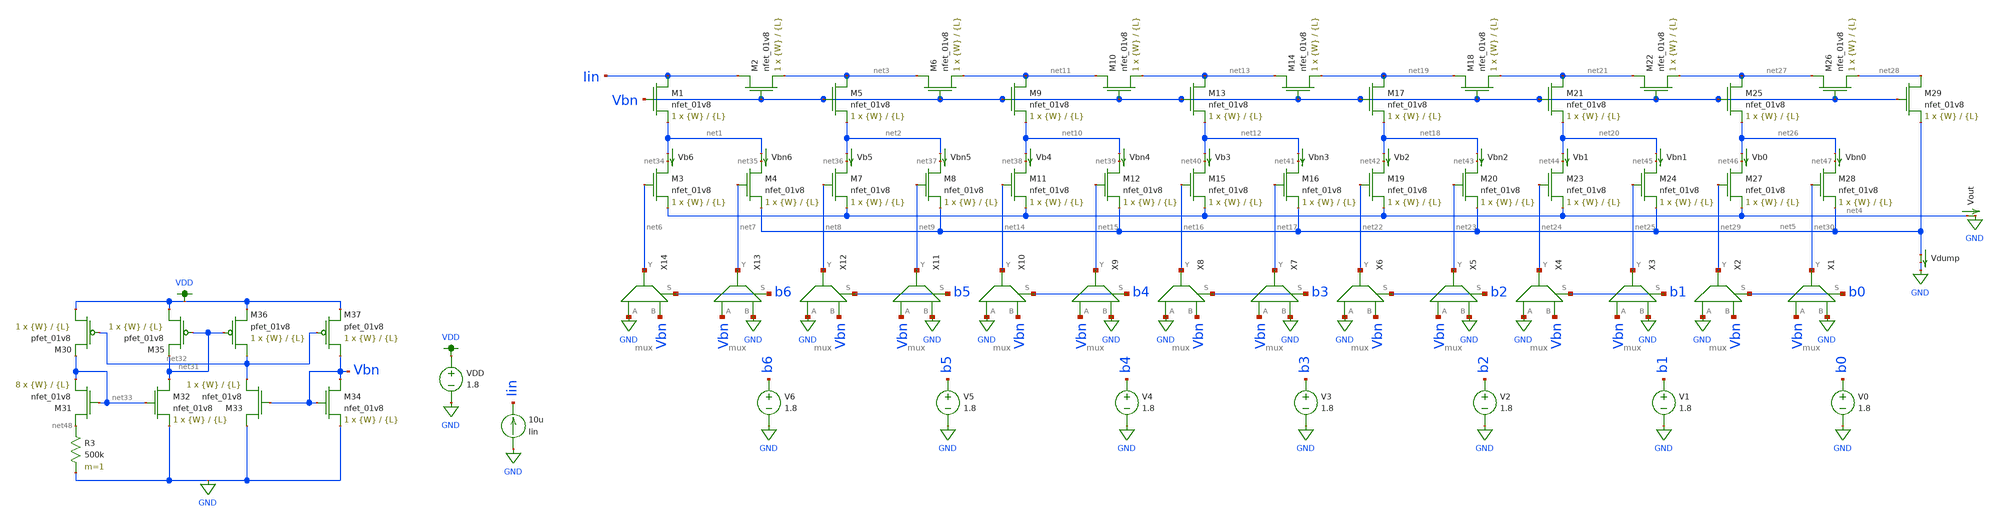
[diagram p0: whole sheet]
** sch_path: schematics/dac_from_paper.sch
**.subckt dac_from_paper
XM1 Iin Vbn net1 GND sky130_fd_pr__nfet_01v8 L={L} W={W} nf=1 ad='int((nf+1)/2) * W/nf * 0.29' as='int((nf+2)/2) * W/nf * 0.29'
+ pd='2*int((nf+1)/2) * (W/nf + 0.29)' ps='2*int((nf+2)/2) * (W/nf + 0.29)' nrd='0.29 / W' nrs='0.29 / W'
+ sa=0 sb=0 sd=0 mult=1 m=1
XM2 Iin Vbn net3 GND sky130_fd_pr__nfet_01v8 L={L} W={W} nf=1 ad='int((nf+1)/2) * W/nf * 0.29' as='int((nf+2)/2) * W/nf * 0.29'
+ pd='2*int((nf+1)/2) * (W/nf + 0.29)' ps='2*int((nf+2)/2) * (W/nf + 0.29)' nrd='0.29 / W' nrs='0.29 / W'
+ sa=0 sb=0 sd=0 mult=1 m=1
XM3 net34 net6 net4 GND sky130_fd_pr__nfet_01v8 L={L} W={W} nf=1 ad='int((nf+1)/2) * W/nf * 0.29' as='int((nf+2)/2) * W/nf * 0.29'
+ pd='2*int((nf+1)/2) * (W/nf + 0.29)' ps='2*int((nf+2)/2) * (W/nf + 0.29)' nrd='0.29 / W' nrs='0.29 / W'
+ sa=0 sb=0 sd=0 mult=1 m=1
XM4 net35 net7 net5 GND sky130_fd_pr__nfet_01v8 L={L} W={W} nf=1 ad='int((nf+1)/2) * W/nf * 0.29' as='int((nf+2)/2) * W/nf * 0.29'
+ pd='2*int((nf+1)/2) * (W/nf + 0.29)' ps='2*int((nf+2)/2) * (W/nf + 0.29)' nrd='0.29 / W' nrs='0.29 / W'
+ sa=0 sb=0 sd=0 mult=1 m=1
XM5 net3 Vbn net2 GND sky130_fd_pr__nfet_01v8 L={L} W={W} nf=1 ad='int((nf+1)/2) * W/nf * 0.29' as='int((nf+2)/2) * W/nf * 0.29'
+ pd='2*int((nf+1)/2) * (W/nf + 0.29)' ps='2*int((nf+2)/2) * (W/nf + 0.29)' nrd='0.29 / W' nrs='0.29 / W'
+ sa=0 sb=0 sd=0 mult=1 m=1
XM6 net3 Vbn net11 GND sky130_fd_pr__nfet_01v8 L={L} W={W} nf=1 ad='int((nf+1)/2) * W/nf * 0.29' as='int((nf+2)/2) * W/nf * 0.29'
+ pd='2*int((nf+1)/2) * (W/nf + 0.29)' ps='2*int((nf+2)/2) * (W/nf + 0.29)' nrd='0.29 / W' nrs='0.29 / W'
+ sa=0 sb=0 sd=0 mult=1 m=1
XM7 net36 net8 net4 GND sky130_fd_pr__nfet_01v8 L={L} W={W} nf=1 ad='int((nf+1)/2) * W/nf * 0.29' as='int((nf+2)/2) * W/nf * 0.29'
+ pd='2*int((nf+1)/2) * (W/nf + 0.29)' ps='2*int((nf+2)/2) * (W/nf + 0.29)' nrd='0.29 / W' nrs='0.29 / W'
+ sa=0 sb=0 sd=0 mult=1 m=1
XM8 net37 net9 net5 GND sky130_fd_pr__nfet_01v8 L={L} W={W} nf=1 ad='int((nf+1)/2) * W/nf * 0.29' as='int((nf+2)/2) * W/nf * 0.29'
+ pd='2*int((nf+1)/2) * (W/nf + 0.29)' ps='2*int((nf+2)/2) * (W/nf + 0.29)' nrd='0.29 / W' nrs='0.29 / W'
+ sa=0 sb=0 sd=0 mult=1 m=1
XM9 net11 Vbn net10 GND sky130_fd_pr__nfet_01v8 L={L} W={W} nf=1 ad='int((nf+1)/2) * W/nf * 0.29' as='int((nf+2)/2) * W/nf * 0.29'
+ pd='2*int((nf+1)/2) * (W/nf + 0.29)' ps='2*int((nf+2)/2) * (W/nf + 0.29)' nrd='0.29 / W' nrs='0.29 / W'
+ sa=0 sb=0 sd=0 mult=1 m=1
XM10 net11 Vbn net13 GND sky130_fd_pr__nfet_01v8 L={L} W={W} nf=1 ad='int((nf+1)/2) * W/nf * 0.29' as='int((nf+2)/2) * W/nf * 0.29'
+ pd='2*int((nf+1)/2) * (W/nf + 0.29)' ps='2*int((nf+2)/2) * (W/nf + 0.29)' nrd='0.29 / W' nrs='0.29 / W'
+ sa=0 sb=0 sd=0 mult=1 m=1
XM11 net38 net14 net4 GND sky130_fd_pr__nfet_01v8 L={L} W={W} nf=1 ad='int((nf+1)/2) * W/nf * 0.29' as='int((nf+2)/2) * W/nf * 0.29'
+ pd='2*int((nf+1)/2) * (W/nf + 0.29)' ps='2*int((nf+2)/2) * (W/nf + 0.29)' nrd='0.29 / W' nrs='0.29 / W'
+ sa=0 sb=0 sd=0 mult=1 m=1
XM12 net39 net15 net5 GND sky130_fd_pr__nfet_01v8 L={L} W={W} nf=1 ad='int((nf+1)/2) * W/nf * 0.29' as='int((nf+2)/2) * W/nf * 0.29'
+ pd='2*int((nf+1)/2) * (W/nf + 0.29)' ps='2*int((nf+2)/2) * (W/nf + 0.29)' nrd='0.29 / W' nrs='0.29 / W'
+ sa=0 sb=0 sd=0 mult=1 m=1
XM13 net13 Vbn net12 GND sky130_fd_pr__nfet_01v8 L={L} W={W} nf=1 ad='int((nf+1)/2) * W/nf * 0.29' as='int((nf+2)/2) * W/nf * 0.29'
+ pd='2*int((nf+1)/2) * (W/nf + 0.29)' ps='2*int((nf+2)/2) * (W/nf + 0.29)' nrd='0.29 / W' nrs='0.29 / W'
+ sa=0 sb=0 sd=0 mult=1 m=1
XM14 net13 Vbn net19 GND sky130_fd_pr__nfet_01v8 L={L} W={W} nf=1 ad='int((nf+1)/2) * W/nf * 0.29' as='int((nf+2)/2) * W/nf * 0.29'
+ pd='2*int((nf+1)/2) * (W/nf + 0.29)' ps='2*int((nf+2)/2) * (W/nf + 0.29)' nrd='0.29 / W' nrs='0.29 / W'
+ sa=0 sb=0 sd=0 mult=1 m=1
XM15 net40 net16 net4 GND sky130_fd_pr__nfet_01v8 L={L} W={W} nf=1 ad='int((nf+1)/2) * W/nf * 0.29' as='int((nf+2)/2) * W/nf * 0.29'
+ pd='2*int((nf+1)/2) * (W/nf + 0.29)' ps='2*int((nf+2)/2) * (W/nf + 0.29)' nrd='0.29 / W' nrs='0.29 / W'
+ sa=0 sb=0 sd=0 mult=1 m=1
XM16 net41 net17 net5 GND sky130_fd_pr__nfet_01v8 L={L} W={W} nf=1 ad='int((nf+1)/2) * W/nf * 0.29' as='int((nf+2)/2) * W/nf * 0.29'
+ pd='2*int((nf+1)/2) * (W/nf + 0.29)' ps='2*int((nf+2)/2) * (W/nf + 0.29)' nrd='0.29 / W' nrs='0.29 / W'
+ sa=0 sb=0 sd=0 mult=1 m=1
XM17 net19 Vbn net18 GND sky130_fd_pr__nfet_01v8 L={L} W={W} nf=1 ad='int((nf+1)/2) * W/nf * 0.29' as='int((nf+2)/2) * W/nf * 0.29'
+ pd='2*int((nf+1)/2) * (W/nf + 0.29)' ps='2*int((nf+2)/2) * (W/nf + 0.29)' nrd='0.29 / W' nrs='0.29 / W'
+ sa=0 sb=0 sd=0 mult=1 m=1
XM18 net19 Vbn net21 GND sky130_fd_pr__nfet_01v8 L={L} W={W} nf=1 ad='int((nf+1)/2) * W/nf * 0.29' as='int((nf+2)/2) * W/nf * 0.29'
+ pd='2*int((nf+1)/2) * (W/nf + 0.29)' ps='2*int((nf+2)/2) * (W/nf + 0.29)' nrd='0.29 / W' nrs='0.29 / W'
+ sa=0 sb=0 sd=0 mult=1 m=1
XM19 net42 net22 net4 GND sky130_fd_pr__nfet_01v8 L={L} W={W} nf=1 ad='int((nf+1)/2) * W/nf * 0.29' as='int((nf+2)/2) * W/nf * 0.29'
+ pd='2*int((nf+1)/2) * (W/nf + 0.29)' ps='2*int((nf+2)/2) * (W/nf + 0.29)' nrd='0.29 / W' nrs='0.29 / W'
+ sa=0 sb=0 sd=0 mult=1 m=1
XM20 net43 net23 net5 GND sky130_fd_pr__nfet_01v8 L={L} W={W} nf=1 ad='int((nf+1)/2) * W/nf * 0.29' as='int((nf+2)/2) * W/nf * 0.29'
+ pd='2*int((nf+1)/2) * (W/nf + 0.29)' ps='2*int((nf+2)/2) * (W/nf + 0.29)' nrd='0.29 / W' nrs='0.29 / W'
+ sa=0 sb=0 sd=0 mult=1 m=1
XM21 net21 Vbn net20 GND sky130_fd_pr__nfet_01v8 L={L} W={W} nf=1 ad='int((nf+1)/2) * W/nf * 0.29' as='int((nf+2)/2) * W/nf * 0.29'
+ pd='2*int((nf+1)/2) * (W/nf + 0.29)' ps='2*int((nf+2)/2) * (W/nf + 0.29)' nrd='0.29 / W' nrs='0.29 / W'
+ sa=0 sb=0 sd=0 mult=1 m=1
XM22 net21 Vbn net27 GND sky130_fd_pr__nfet_01v8 L={L} W={W} nf=1 ad='int((nf+1)/2) * W/nf * 0.29' as='int((nf+2)/2) * W/nf * 0.29'
+ pd='2*int((nf+1)/2) * (W/nf + 0.29)' ps='2*int((nf+2)/2) * (W/nf + 0.29)' nrd='0.29 / W' nrs='0.29 / W'
+ sa=0 sb=0 sd=0 mult=1 m=1
XM23 net44 net24 net4 GND sky130_fd_pr__nfet_01v8 L={L} W={W} nf=1 ad='int((nf+1)/2) * W/nf * 0.29' as='int((nf+2)/2) * W/nf * 0.29'
+ pd='2*int((nf+1)/2) * (W/nf + 0.29)' ps='2*int((nf+2)/2) * (W/nf + 0.29)' nrd='0.29 / W' nrs='0.29 / W'
+ sa=0 sb=0 sd=0 mult=1 m=1
XM24 net45 net25 net5 GND sky130_fd_pr__nfet_01v8 L={L} W={W} nf=1 ad='int((nf+1)/2) * W/nf * 0.29' as='int((nf+2)/2) * W/nf * 0.29'
+ pd='2*int((nf+1)/2) * (W/nf + 0.29)' ps='2*int((nf+2)/2) * (W/nf + 0.29)' nrd='0.29 / W' nrs='0.29 / W'
+ sa=0 sb=0 sd=0 mult=1 m=1
XM25 net27 Vbn net26 GND sky130_fd_pr__nfet_01v8 L={L} W={W} nf=1 ad='int((nf+1)/2) * W/nf * 0.29' as='int((nf+2)/2) * W/nf * 0.29'
+ pd='2*int((nf+1)/2) * (W/nf + 0.29)' ps='2*int((nf+2)/2) * (W/nf + 0.29)' nrd='0.29 / W' nrs='0.29 / W'
+ sa=0 sb=0 sd=0 mult=1 m=1
XM26 net27 Vbn net28 GND sky130_fd_pr__nfet_01v8 L={L} W={W} nf=1 ad='int((nf+1)/2) * W/nf * 0.29' as='int((nf+2)/2) * W/nf * 0.29'
+ pd='2*int((nf+1)/2) * (W/nf + 0.29)' ps='2*int((nf+2)/2) * (W/nf + 0.29)' nrd='0.29 / W' nrs='0.29 / W'
+ sa=0 sb=0 sd=0 mult=1 m=1
XM27 net46 net29 net4 GND sky130_fd_pr__nfet_01v8 L={L} W={W} nf=1 ad='int((nf+1)/2) * W/nf * 0.29' as='int((nf+2)/2) * W/nf * 0.29'
+ pd='2*int((nf+1)/2) * (W/nf + 0.29)' ps='2*int((nf+2)/2) * (W/nf + 0.29)' nrd='0.29 / W' nrs='0.29 / W'
+ sa=0 sb=0 sd=0 mult=1 m=1
XM28 net47 net30 net5 GND sky130_fd_pr__nfet_01v8 L={L} W={W} nf=1 ad='int((nf+1)/2) * W/nf * 0.29' as='int((nf+2)/2) * W/nf * 0.29'
+ pd='2*int((nf+1)/2) * (W/nf + 0.29)' ps='2*int((nf+2)/2) * (W/nf + 0.29)' nrd='0.29 / W' nrs='0.29 / W'
+ sa=0 sb=0 sd=0 mult=1 m=1
XM29 net28 Vbn net5 GND sky130_fd_pr__nfet_01v8 L={L} W={W} nf=1 ad='int((nf+1)/2) * W/nf * 0.29' as='int((nf+2)/2) * W/nf * 0.29'
+ pd='2*int((nf+1)/2) * (W/nf + 0.29)' ps='2*int((nf+2)/2) * (W/nf + 0.29)' nrd='0.29 / W' nrs='0.29 / W'
+ sa=0 sb=0 sd=0 mult=1 m=1
Vdump net5 GND 0
.save i(vdump)
Vb0 net26 net46 0
.save i(vb0)
Vbn0 net26 net47 0
.save i(vbn0)
Vb5 net2 net36 0
.save i(vb5)
Vb6 net1 net34 0
.save i(vb6)
Iin GND Iin 10u
Vout net4 GND 0
.save i(vout)
Vb1 net20 net44 0
.save i(vb1)
Vb2 net18 net42 0
.save i(vb2)
Vb3 net12 net40 0
.save i(vb3)
Vb4 net10 net38 0
.save i(vb4)
Vbn1 net20 net45 0
.save i(vbn1)
Vbn2 net18 net43 0
.save i(vbn2)
Vbn3 net12 net41 0
.save i(vbn3)
Vbn4 net10 net39 0
.save i(vbn4)
Vbn5 net2 net37 0
.save i(vbn5)
Vbn6 net1 net35 0
.save i(vbn6)
V0 b0 GND 1.8
V1 b1 GND 1.8
V2 b2 GND 1.8
V3 b3 GND 1.8
V4 b4 GND 1.8
V5 b5 GND 1.8
V6 b6 GND 1.8
X1 Vbn GND net30 b0 mux
X2 GND Vbn net29 b0 mux
X3 Vbn GND net25 b1 mux
X4 GND Vbn net24 b1 mux
X5 Vbn GND net23 b2 mux
X6 GND Vbn net22 b2 mux
X7 Vbn GND net17 b3 mux
X8 GND Vbn net16 b3 mux
X9 Vbn GND net15 b4 mux
X10 GND Vbn net14 b4 mux
X11 Vbn GND net9 b5 mux
X12 GND Vbn net8 b5 mux
X13 Vbn GND net7 b6 mux
X14 GND Vbn net6 b6 mux
XM30 VDD net32 net33 VDD sky130_fd_pr__pfet_01v8 L={L} W={W} nf=1 ad='int((nf+1)/2) * W/nf * 0.29' as='int((nf+2)/2) * W/nf * 0.29'
+ pd='2*int((nf+1)/2) * (W/nf + 0.29)' ps='2*int((nf+2)/2) * (W/nf + 0.29)' nrd='0.29 / W' nrs='0.29 / W'
+ sa=0 sb=0 sd=0 mult=1 m=1
XM31 net48 net33 net33 GND sky130_fd_pr__nfet_01v8 L={L} W={W} nf=1 ad='int((nf+1)/2) * W/nf * 0.29'
+ as='int((nf+2)/2) * W/nf * 0.29' pd='2*int((nf+1)/2) * (W/nf + 0.29)' ps='2*int((nf+2)/2) * (W/nf + 0.29)'
+ nrd='0.29 / W' nrs='0.29 / W' sa=0 sb=0 sd=0 mult=8 m=8
R3 net48 GND 500k m=1
XM32 net31 net33 GND GND sky130_fd_pr__nfet_01v8 L={L} W={W} nf=1 ad='int((nf+1)/2) * W/nf * 0.29' as='int((nf+2)/2) * W/nf * 0.29'
+ pd='2*int((nf+1)/2) * (W/nf + 0.29)' ps='2*int((nf+2)/2) * (W/nf + 0.29)' nrd='0.29 / W' nrs='0.29 / W'
+ sa=0 sb=0 sd=0 mult=1 m=1
XM33 GND Vbn net32 GND sky130_fd_pr__nfet_01v8 L={L} W={W} nf=1 ad='int((nf+1)/2) * W/nf * 0.29' as='int((nf+2)/2) * W/nf * 0.29'
+ pd='2*int((nf+1)/2) * (W/nf + 0.29)' ps='2*int((nf+2)/2) * (W/nf + 0.29)' nrd='0.29 / W' nrs='0.29 / W'
+ sa=0 sb=0 sd=0 mult=1 m=1
XM34 Vbn Vbn GND GND sky130_fd_pr__nfet_01v8 L={L} W={W} nf=1 ad='int((nf+1)/2) * W/nf * 0.29' as='int((nf+2)/2) * W/nf * 0.29'
+ pd='2*int((nf+1)/2) * (W/nf + 0.29)' ps='2*int((nf+2)/2) * (W/nf + 0.29)' nrd='0.29 / W' nrs='0.29 / W'
+ sa=0 sb=0 sd=0 mult=1 m=1
XM35 VDD net31 net31 VDD sky130_fd_pr__pfet_01v8 L={L} W={W} nf=1 ad='int((nf+1)/2) * W/nf * 0.29' as='int((nf+2)/2) * W/nf * 0.29'
+ pd='2*int((nf+1)/2) * (W/nf + 0.29)' ps='2*int((nf+2)/2) * (W/nf + 0.29)' nrd='0.29 / W' nrs='0.29 / W'
+ sa=0 sb=0 sd=0 mult=1 m=1
XM36 net32 net31 VDD VDD sky130_fd_pr__pfet_01v8 L={L} W={W} nf=1 ad='int((nf+1)/2) * W/nf * 0.29' as='int((nf+2)/2) * W/nf * 0.29'
+ pd='2*int((nf+1)/2) * (W/nf + 0.29)' ps='2*int((nf+2)/2) * (W/nf + 0.29)' nrd='0.29 / W' nrs='0.29 / W'
+ sa=0 sb=0 sd=0 mult=1 m=1
XM37 Vbn net32 VDD VDD sky130_fd_pr__pfet_01v8 L={L} W={W} nf=1 ad='int((nf+1)/2) * W/nf * 0.29' as='int((nf+2)/2) * W/nf * 0.29'
+ pd='2*int((nf+1)/2) * (W/nf + 0.29)' ps='2*int((nf+2)/2) * (W/nf + 0.29)' nrd='0.29 / W' nrs='0.29 / W'
+ sa=0 sb=0 sd=0 mult=1 m=1
VDD VDD GND 1.8
**** begin user architecture code

.option wnflag=1
.param MC_SWITCH=1.0
.lib ~/skywater/skywater-pdk/libraries/sky130_fd_pr_ngspice/latest/models/sky130.lib.spice tt


.param W=12
.param L=4
.control
set wr_vecnames
set wr_singlescale
let code = 0
  while code < 128
    if code eq 0
      let b0 = 0
    else
      let b0 = code % 2
    end
    if floor(code / 2) eq 0
      let b1 = 0
    else
      let b1 = floor(code / 2) % 2
    end
    if floor(code / 4) eq 0
      let b2 = 0
    else
      let b2 = floor(code / 4) % 2
    end
    if floor(code / 8) eq 0
      let b3 = 0
    else
      let b3 = floor(code / 8) % 2
    end
    if floor(code / 16) eq 0
      let b4 = 0
    else
      let b4 = floor(code / 16) % 2
    end
    if floor(code / 32) eq 0
      let b5 = 0
    else
      let b5 = floor(code / 32) % 2
    end
    if floor(code / 64) eq 0
      let b6 = 0
    else
      let b6 = floor(code / 64) % 2
    end
    alter v0 $&b0
    alter v1 $&b1
    alter v2 $&b2
    alter v3 $&b3
    alter v4 $&b4
    alter v5 $&b5
    alter v6 $&b6
    save all
    op
    wrdata ~/Documents/current-output-dac-vlsi/simulations/dac_paper_sim.txt i(vb0) i(vb1) i(vb2)
+ i(vb3) i(vb4) i(vb5) i(vb6) i(Vout) i(Vdump)
    if code eq 0
      set appendwrite
      set wr_vecnames = FALSE
    end
    let code = code + 1
  end
  quit
.endc

**** end user architecture code
**.ends

* expanding   symbol:  /home/madvlsi/Documents/current-output-dac-vlsi/schematics/mux.sym # of
*+ pins=4
** sym_path: /home/madvlsi/Documents/current-output-dac-vlsi/schematics/mux.sym
** sch_path: /home/madvlsi/Documents/current-output-dac-vlsi/schematics/mux.sch
.subckt mux A B Y S
*.ipin S
*.ipin A
*.opin Y
*.ipin B
XM1 net1 S GND GND sky130_fd_pr__nfet_01v8 L=0.15 W=1 nf=1 ad='int((nf+1)/2) * W/nf * 0.29' as='int((nf+2)/2) * W/nf * 0.29'
+ pd='2*int((nf+1)/2) * (W/nf + 0.29)' ps='2*int((nf+2)/2) * (W/nf + 0.29)' nrd='0.29 / W' nrs='0.29 / W'
+ sa=0 sb=0 sd=0 mult=1 m=1
XM2 net1 S VDD VDD sky130_fd_pr__pfet_01v8 L=0.15 W=1 nf=1 ad='int((nf+1)/2) * W/nf * 0.29' as='int((nf+2)/2) * W/nf * 0.29'
+ pd='2*int((nf+1)/2) * (W/nf + 0.29)' ps='2*int((nf+2)/2) * (W/nf + 0.29)' nrd='0.29 / W' nrs='0.29 / W'
+ sa=0 sb=0 sd=0 mult=1 m=1
XM3 Y S B GND sky130_fd_pr__nfet_01v8 L=0.15 W=1 nf=1 ad='int((nf+1)/2) * W/nf * 0.29' as='int((nf+2)/2) * W/nf * 0.29'
+ pd='2*int((nf+1)/2) * (W/nf + 0.29)' ps='2*int((nf+2)/2) * (W/nf + 0.29)' nrd='0.29 / W' nrs='0.29 / W'
+ sa=0 sb=0 sd=0 mult=1 m=1
XM4 A net1 Y GND sky130_fd_pr__nfet_01v8 L=0.15 W=1 nf=1 ad='int((nf+1)/2) * W/nf * 0.29' as='int((nf+2)/2) * W/nf * 0.29'
+ pd='2*int((nf+1)/2) * (W/nf + 0.29)' ps='2*int((nf+2)/2) * (W/nf + 0.29)' nrd='0.29 / W' nrs='0.29 / W'
+ sa=0 sb=0 sd=0 mult=1 m=1
.ends

.GLOBAL GND
.GLOBAL VDD
.end
